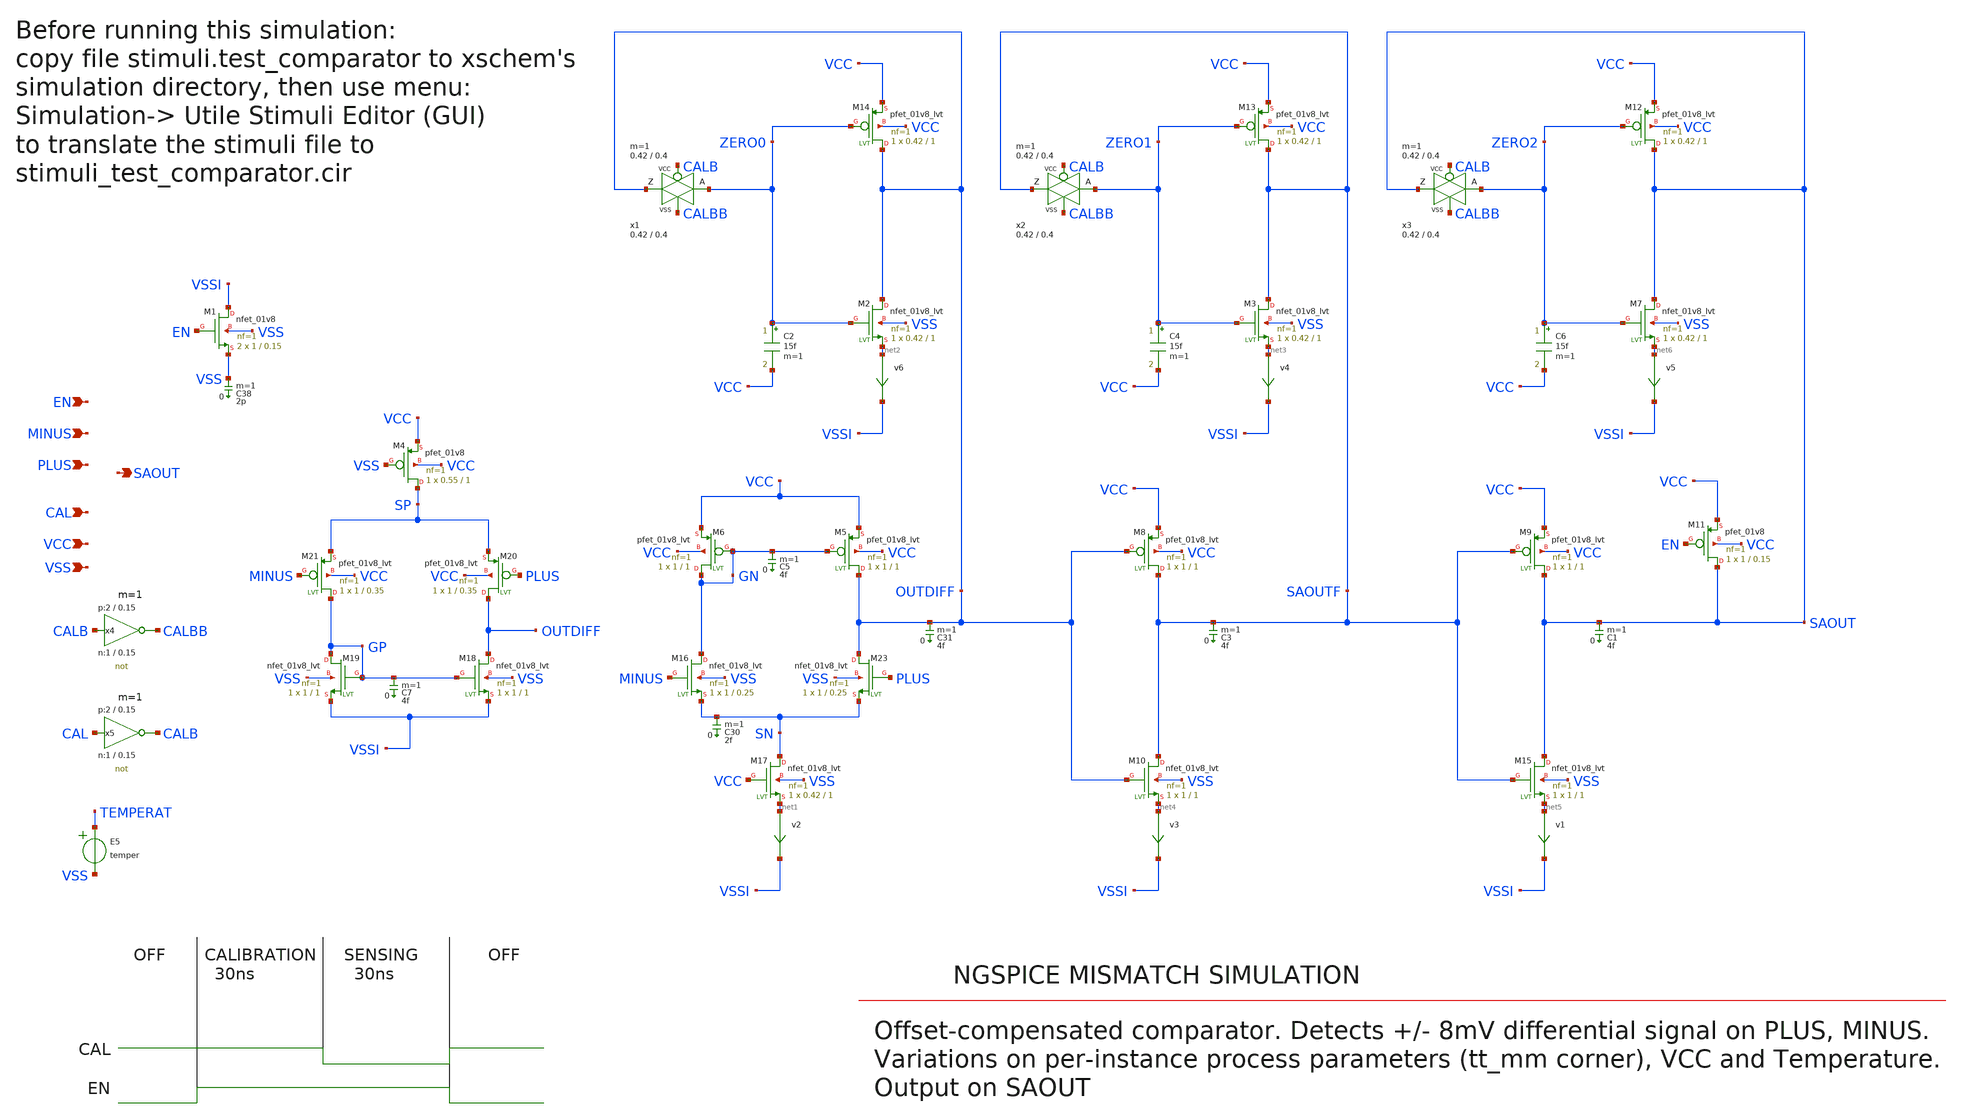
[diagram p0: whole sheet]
** sch_path: sky130_tests/test_comparator.sch
* Copyright 2021 Stefan Frederik Schippers
* Licensed under the Apache License, Version 2.0 (the "License");
* you may not use this file except in compliance with the License.
* You may obtain a copy of the License at
* https://www.apache.org/licenses/LICENSE-2.0
* Unless required by applicable law or agreed to in writing, software
* distributed under the License is distributed on an "AS IS" BASIS,
* WITHOUT WARRANTIES OR CONDITIONS OF ANY KIND, either express or implied.
* See the License for the specific language governing permissions and
* limitations under the License.
* sky130_tests/not.sym:
* Copyright 2020 Stefan Frederik Schippers
**.subckt test_comparator CAL PLUS MINUS EN VSS VCC SAOUT
*.ipin CAL
*.ipin PLUS
*.ipin MINUS
*.ipin EN
*.ipin VSS
*.ipin VCC
*.opin SAOUT
E5 TEMPERAT VSS VOL=' temper '
C38 VSS 0 2p m=1
C3 SAOUTF 0 4f m=1
C5 GN 0 4f m=1
C30 SN 0 2f m=1
C31 OUTDIFF 0 4f m=1
v2 net1 VSSI 0
.save i(v2)
v3 net4 VSSI 0
.save i(v3)
v4 net3 VSSI 0
.save i(v4)
v6 net2 VSSI 0
.save i(v6)
C1 SAOUT 0 4f m=1
v1 net5 VSSI 0
.save i(v1)
v5 net6 VSSI 0
.save i(v5)
C7 GP 0 4f m=1
x4 CALBB CALB VCC VSS not W_N=1 L_N=0.15 W_P=2 L_P=0.15 m=1
x5 CALB CAL VCC VSS not W_N=1 L_N=0.15 W_P=2 L_P=0.15 m=1
XM4 SP VSS VCC VCC sky130_fd_pr__pfet_01v8 L=1 W=0.55 nf=1 ad='W * 0.29' as='W * 0.29' pd='W + 2 * 0.29'
+ ps='W + 2 * 0.29' nrd=0 nrs=0 sa=0 sb=0 sd=0 mult=1 m=1
XM5 OUTDIFF GN VCC VCC sky130_fd_pr__pfet_01v8_lvt L=1 W=1 nf=1 ad='W * 0.29' as='W * 0.29' pd='2*(W + 0.29)'
+ ps='2*(W + 0.29)' nrd=0 nrs=0 sa=0 sb=0 sd=0 mult=1 m=1
XM6 GN GN VCC VCC sky130_fd_pr__pfet_01v8_lvt L=1 W=1 nf=1 ad='W * 0.29' as='W * 0.29' pd='2*(W + 0.29)'
+ ps='2*(W + 0.29)' nrd=0 nrs=0 sa=0 sb=0 sd=0 mult=1 m=1
XM8 SAOUTF OUTDIFF VCC VCC sky130_fd_pr__pfet_01v8_lvt L=1 W=1 nf=1 ad='W * 0.29' as='W * 0.29' pd='2*(W + 0.29)'
+ ps='2*(W + 0.29)' nrd=0 nrs=0 sa=0 sb=0 sd=0 mult=1 m=1
XM9 SAOUT SAOUTF VCC VCC sky130_fd_pr__pfet_01v8_lvt L=1 W=1 nf=1 ad='W * 0.29' as='W * 0.29' pd='2*(W + 0.29)'
+ ps='2*(W + 0.29)' nrd=0 nrs=0 sa=0 sb=0 sd=0 mult=1 m=1
XM11 SAOUT EN VCC VCC sky130_fd_pr__pfet_01v8 L=0.15 W=1 nf=1 ad='W * 0.29' as='W * 0.29' pd='W + 2 * 0.29'
+ ps='W + 2 * 0.29' nrd=0 nrs=0 sa=0 sb=0 sd=0 mult=1 m=1
XM12 SAOUT ZERO2 VCC VCC sky130_fd_pr__pfet_01v8_lvt L=1 W=0.42 nf=1 ad='W * 0.29' as='W * 0.29' pd='2*(W + 0.29)'
+ ps='2*(W + 0.29)' nrd=0 nrs=0 sa=0 sb=0 sd=0 mult=1 m=1
XM13 SAOUTF ZERO1 VCC VCC sky130_fd_pr__pfet_01v8_lvt L=1 W=0.42 nf=1 ad='W * 0.29' as='W * 0.29' pd='2*(W + 0.29)'
+ ps='2*(W + 0.29)' nrd=0 nrs=0 sa=0 sb=0 sd=0 mult=1 m=1
XM14 OUTDIFF ZERO0 VCC VCC sky130_fd_pr__pfet_01v8_lvt L=1 W=0.42 nf=1 ad='W * 0.29' as='W * 0.29' pd='2*(W + 0.29)'
+ ps='2*(W + 0.29)' nrd=0 nrs=0 sa=0 sb=0 sd=0 mult=1 m=1
XM1 VSSI EN VSS VSS sky130_fd_pr__nfet_01v8 L=0.15 W=1 nf=1 ad='W * 0.29' as='W * 0.29' pd='W + 2 * 0.29'
+ ps='W + 2 * 0.29' nrd=0 nrs=0 sa=0 sb=0 sd=0 mult=2 m=2
XM2 OUTDIFF ZERO0 net2 VSS sky130_fd_pr__nfet_01v8_lvt L=1 W=0.42 nf=1 ad='W * 0.29' as='W * 0.29' pd='2*(W + 0.29)'
+ ps='2*(W + 0.29)' nrd=0 nrs=0 sa=0 sb=0 sd=0 mult=1 m=1
XM3 SAOUTF ZERO1 net3 VSS sky130_fd_pr__nfet_01v8_lvt L=1 W=0.42 nf=1 ad='W * 0.29' as='W * 0.29' pd='2*(W + 0.29)'
+ ps='2*(W + 0.29)' nrd=0 nrs=0 sa=0 sb=0 sd=0 mult=1 m=1
XM7 SAOUT ZERO2 net6 VSS sky130_fd_pr__nfet_01v8_lvt L=1 W=0.42 nf=1 ad='W * 0.29' as='W * 0.29' pd='2*(W + 0.29)'
+ ps='2*(W + 0.29)' nrd=0 nrs=0 sa=0 sb=0 sd=0 mult=1 m=1
XM15 SAOUT SAOUTF net5 VSS sky130_fd_pr__nfet_01v8_lvt L=1 W=1 nf=1 ad='W * 0.29' as='W * 0.29' pd='2*(W + 0.29)'
+ ps='2*(W + 0.29)' nrd=0 nrs=0 sa=0 sb=0 sd=0 mult=1 m=1
XM10 SAOUTF OUTDIFF net4 VSS sky130_fd_pr__nfet_01v8_lvt L=1 W=1 nf=1 ad='W * 0.29' as='W * 0.29' pd='2*(W + 0.29)'
+ ps='2*(W + 0.29)' nrd=0 nrs=0 sa=0 sb=0 sd=0 mult=1 m=1
XM17 SN VCC net1 VSS sky130_fd_pr__nfet_01v8_lvt L=1 W=0.42 nf=1 ad='W * 0.29' as='W * 0.29' pd='2*(W + 0.29)'
+ ps='2*(W + 0.29)' nrd=0 nrs=0 sa=0 sb=0 sd=0 mult=1 m=1
XM18 OUTDIFF GP VSSI VSS sky130_fd_pr__nfet_01v8_lvt L=1 W=1 nf=1 ad='W * 0.29' as='W * 0.29' pd='2*(W + 0.29)'
+ ps='2*(W + 0.29)' nrd=0 nrs=0 sa=0 sb=0 sd=0 mult=1 m=1
XM19 GP GP VSSI VSS sky130_fd_pr__nfet_01v8_lvt L=1 W=1 nf=1 ad='W * 0.29' as='W * 0.29' pd='2*(W + 0.29)'
+ ps='2*(W + 0.29)' nrd=0 nrs=0 sa=0 sb=0 sd=0 mult=1 m=1
XM20 OUTDIFF PLUS SP VCC sky130_fd_pr__pfet_01v8_lvt L=0.35 W=1 nf=1 ad='W * 0.29' as='W * 0.29' pd='2*(W + 0.29)'
+ ps='2*(W + 0.29)' nrd=0 nrs=0 sa=0 sb=0 sd=0 mult=1 m=1
XM21 GP MINUS SP VCC sky130_fd_pr__pfet_01v8_lvt L=0.35 W=1 nf=1 ad='W * 0.29' as='W * 0.29' pd='2*(W + 0.29)'
+ ps='2*(W + 0.29)' nrd=0 nrs=0 sa=0 sb=0 sd=0 mult=1 m=1
XM23 OUTDIFF PLUS SN VSS sky130_fd_pr__nfet_01v8_lvt L=0.25 W=1 nf=1 ad='W * 0.29' as='W * 0.29' pd='2*(W + 0.29)'
+ ps='2*(W + 0.29)' nrd=0 nrs=0 sa=0 sb=0 sd=0 mult=1 m=1
XM16 GN MINUS SN VSS sky130_fd_pr__nfet_01v8_lvt L=0.25 W=1 nf=1 ad='W * 0.29' as='W * 0.29' pd='2*(W + 0.29)'
+ ps='2*(W + 0.29)' nrd=0 nrs=0 sa=0 sb=0 sd=0 mult=1 m=1
x1 OUTDIFF ZERO0 CALB CALBB VCC VSS passgate_nlvt W_N=0.42 L_N=0.4 W_P=0.42 L_P=0.4 ad=0 as=0 pd=0
+ ps=1
x2 SAOUTF ZERO1 CALB CALBB VCC VSS passgate_nlvt W_N=0.42 L_N=0.4 W_P=0.42 L_P=0.4 ad=0 as=0 pd=0
+ ps=1
x3 SAOUT ZERO2 CALB CALBB VCC VSS passgate_nlvt W_N=0.42 L_N=0.4 W_P=0.42 L_P=0.4 ad=0 as=0 pd=0
+ ps=1
C2 ZERO0 VCC 15f m=1
C4 ZERO1 VCC 15f m=1
C6 ZERO2 VCC 15f m=1
**** begin user architecture code

** opencircuitdesign pdks install
.lib $::SKYWATER_MODELS/sky130.lib.spice tt_mm


**** end user architecture code
**.ends

* expanding   symbol:  sky130_tests/not.sym # of pins=2
** sym_path: sky130_tests/not.sym
** sch_path: sky130_tests/not.sch
.subckt not y a VCCPIN VSSPIN     W_N=1 L_N=0.15 W_P=2 L_P=0.15
*.opin y
*.ipin a
XM1 DN a VSSPIN VSSPIN sky130_fd_pr__nfet_01v8 L=L_N W=W_N nf=1 ad='int((nf+1)/2) * W/nf * 0.29' as='int((nf+2)/2) * W/nf * 0.29'
+ pd='2*int((nf+1)/2) * (W/nf + 0.29)' ps='2*int((nf+2)/2) * (W/nf + 0.29)' nrd='0.29 / W' nrs='0.29 / W'
+ sa=0 sb=0 sd=0 mult=1 m=1
XM2 DP a VCCPIN VCCPIN sky130_fd_pr__pfet_01v8 L=L_P W=W_P nf=1 ad='int((nf+1)/2) * W/nf * 0.29' as='int((nf+2)/2) * W/nf * 0.29'
+ pd='2*int((nf+1)/2) * (W/nf + 0.29)' ps='2*int((nf+2)/2) * (W/nf + 0.29)' nrd='0.29 / W' nrs='0.29 / W'
+ sa=0 sb=0 sd=0 mult=1 m=1
Vmeas DP y 0
.save i(vmeas)
Vmeas1 y DN 0
.save i(vmeas1)
.save v(dp)
.save v(dn)
.ends


* expanding   symbol:  sky130_tests/passgate_nlvt.sym # of pins=4
** sym_path: sky130_tests/passgate_nlvt.sym
** sch_path: sky130_tests/passgate_nlvt.sch
.subckt passgate_nlvt Z A GP GN VCCBPIN VSSBPIN  W_N=1 L_N=0.2 W_P=1 L_P=0.2   ad=0 as=0 pd=0 ps=0
*.iopin A
*.iopin Z
*.ipin GP
*.ipin GN
XM1 net1 GN net2 VSS sky130_fd_pr__nfet_01v8_lvt L=L_N W=W_N nf=1 ad=ad as=as pd=pd ps=ps nrd=0
+ nrs=0 sa=0 sb=0 sd=0 mult=1 m=1
XM2 A GP Z VCC sky130_fd_pr__pfet_01v8 W=W_P L=L_P ad=ad pd=pd as=as ps=ps nrd=0 nrs=0 sa=0 sb=0
+ sd=0 nf=1 mult=1
.ends

**** begin user architecture code


** this experimental option enables mos model bin
** selection based on W/NF instead of W
.option wnflag=1

.param VCCGAUSS=agauss(1.8, 0.05, 1)
.param VCC='VCCGAUSS'
** use following line to remove VCC variations
* .param VCC=1.8
.param VDL='VCC/2+0.2'
.param TEMPGAUSS=agauss(40, 30, 1)
.option temp='TEMPGAUSS'
** use following line to remove temperature variations
* .option temp=25

** to generate following file:
** copy .../xschem_sky130/sky130_tests/stimuli.test_comparator to simulation directory
** then do 'Simulation->Utile Stimuli Editor (GUI)' and press 'Translate'
.include "stimuli_test_comparator.cir"

.control
  option seed=12
  let run=1
  dowhile run <= 40
    if run > 1
      reset
      set appendwrite
    end
    save all
    * save saout cal i(vvcc) en plus minus
    tran 0.1n 300n uic
    write test_comparator.raw
    let run = run + 1
  end
.endc


**** end user architecture code
.end
